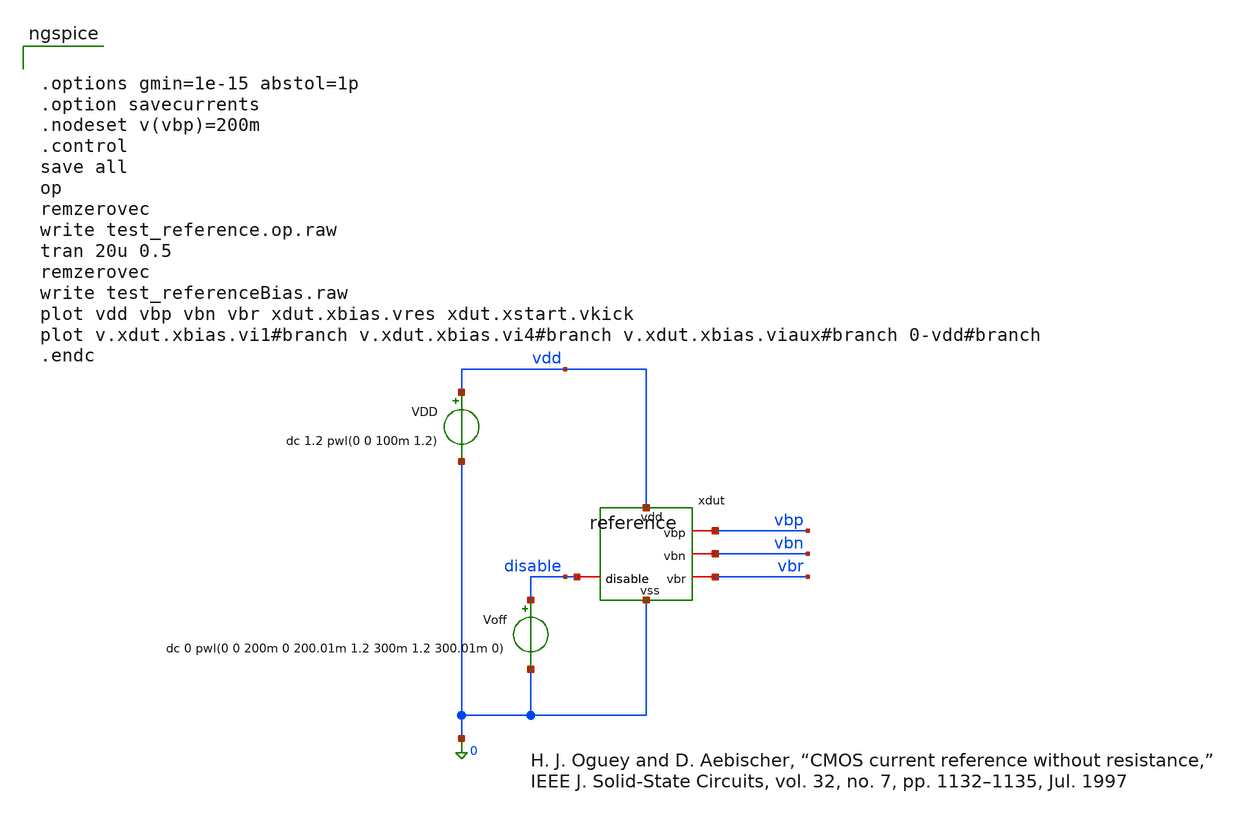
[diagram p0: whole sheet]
** sch_path: xschem/test_reference.sch
**.subckt test_reference
xdut vdd vbp vbn disable vbr 0 reference
VDD vdd 0 dc 1.2 pwl(0 0 100m 1.2)
Voff disable 0 dc 0 pwl(0 0 200m 0 200.01m 1.2 300m 1.2 300.01m 0)
**** begin user architecture code


.options gmin=1e-15 abstol=1p
.option savecurrents
.nodeset v(vbp)=200m
.control
save all
op
remzerovec
write test_reference.op.raw
tran 20u 0.5
remzerovec
write test_referenceBias.raw
plot vdd vbp vbn vbr xdut.xbias.vres xdut.xstart.vkick
plot v.xdut.xbias.vi1#branch v.xdut.xbias.vi4#branch v.xdut.xbias.viaux#branch 0-vdd#branch
.endc


 .lib cornerMOShv.lib mos_tt

.param mc_mm_switch=0
.param mc_pr_switch=1


**** end user architecture code
**.ends
.end
